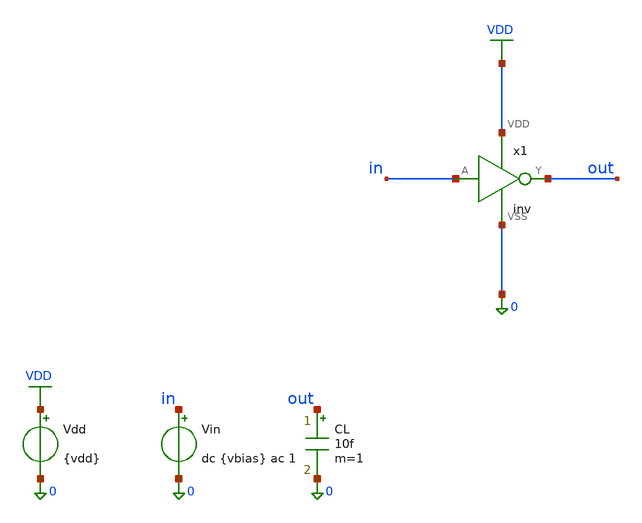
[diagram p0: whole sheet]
** sch_path: examples/ihp-inv/libs/cells/tb_inv_ac/schematic/tb_inv_ac.sch
**.subckt tb_inv_ac
x1 in out VDD 0 inv
Vdd VDD 0 {vdd}
Vin in 0 dc {vbias} ac 1
CL out 0 10f m=1
**.ends
.GLOBAL VDD
.end
